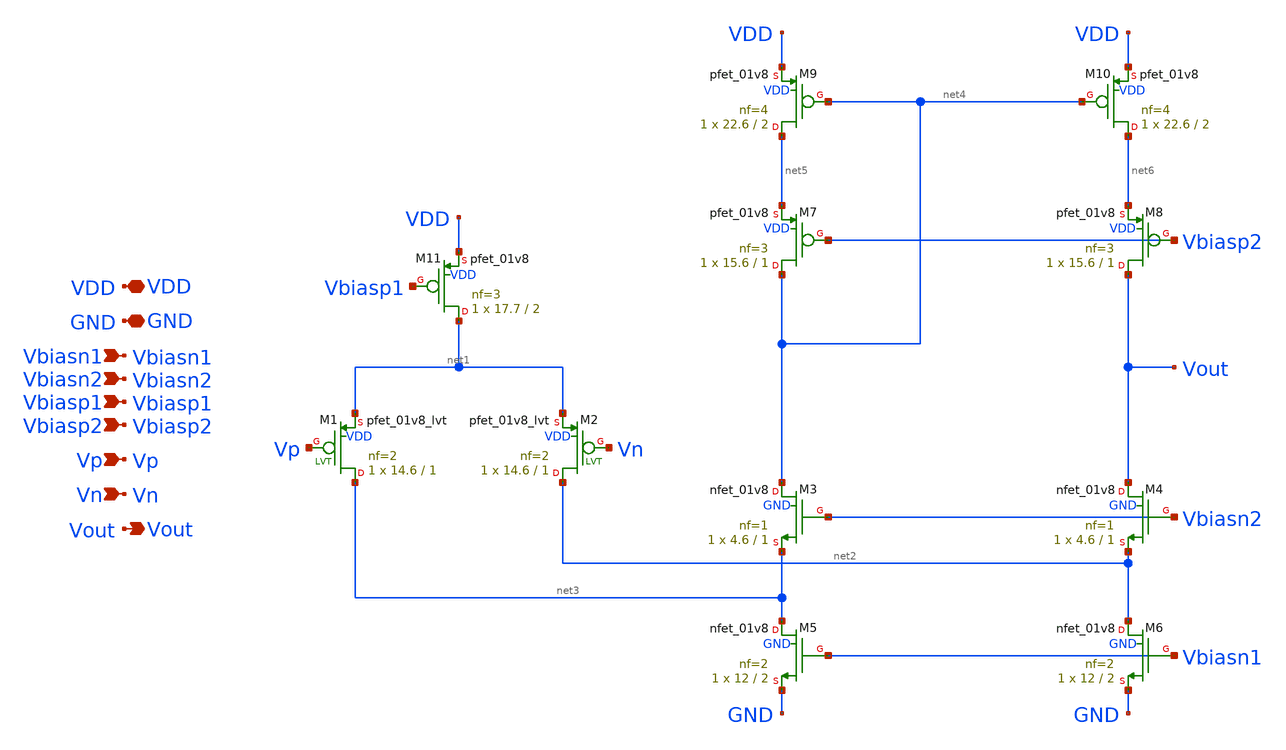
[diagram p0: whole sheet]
** sch_path: sch/vi_converter/ota_vi.sch
**.subckt ota_vi Vbiasn2 Vout VDD GND Vp Vn Vbiasp1 Vbiasp2 Vbiasn1
*.ipin Vbiasn2
*.opin Vout
*.iopin VDD
*.iopin GND
*.ipin Vp
*.ipin Vn
*.ipin Vbiasp1
*.ipin Vbiasp2
*.ipin Vbiasn1
XM3 net4 Vbiasn2 net3 GND sky130_fd_pr__nfet_01v8 L=1 W=4.6 nf=1 ad='int((1 + 1)/2) * 4.6 / 1 * 0.29'
+ as='int((1 + 2)/2) * 4.6 / 1 * 0.29' pd='2*int((1 + 1)/2) * (4.6 / 1 + 0.29)' ps='2*int((1 + 2)/2) * (4.6 / 1 + 0.29)'
+ nrd='0.29 / 4.6 ' nrs='0.29 / 4.6 ' sa=0 sb=0 sd=0 mult=1 m=1
XM4 Vout Vbiasn2 net2 GND sky130_fd_pr__nfet_01v8 L=1 W=4.6 nf=1 ad='int((1 + 1)/2) * 4.6 / 1 * 0.29'
+ as='int((1 + 2)/2) * 4.6 / 1 * 0.29' pd='2*int((1 + 1)/2) * (4.6 / 1 + 0.29)' ps='2*int((1 + 2)/2) * (4.6 / 1 + 0.29)'
+ nrd='0.29 / 4.6 ' nrs='0.29 / 4.6 ' sa=0 sb=0 sd=0 mult=1 m=1
XM5 net3 Vbiasn1 GND GND sky130_fd_pr__nfet_01v8 L=2 W=12 nf=2 ad='int((2 + 1)/2) * 12 / 2 * 0.29' as='int((2 + 2)/2) * 12 / 2 * 0.29'
+ pd='2*int((2 + 1)/2) * (12 / 2 + 0.29)' ps='2*int((2 + 2)/2) * (12 / 2 + 0.29)' nrd='0.29 / 12 ' nrs='0.29 / 12 '
+ sa=0 sb=0 sd=0 mult=1 m=1
XM6 net2 Vbiasn1 GND GND sky130_fd_pr__nfet_01v8 L=2 W=12 nf=2 ad='int((2 + 1)/2) * 12 / 2 * 0.29' as='int((2 + 2)/2) * 12 / 2 * 0.29'
+ pd='2*int((2 + 1)/2) * (12 / 2 + 0.29)' ps='2*int((2 + 2)/2) * (12 / 2 + 0.29)' nrd='0.29 / 12 ' nrs='0.29 / 12 '
+ sa=0 sb=0 sd=0 mult=1 m=1
XM7 net4 Vbiasp2 net5 VDD sky130_fd_pr__pfet_01v8 L=1 W=15.6 nf=3 ad='int((3 + 1)/2) * 15.6 / 3 * 0.29'
+ as='int((3 + 2)/2) * 15.6 / 3 * 0.29' pd='2*int((3 + 1)/2) * (15.6 / 3 + 0.29)' ps='2*int((3 + 2)/2) * (15.6 / 3 + 0.29)'
+ nrd='0.29 / 15.6 ' nrs='0.29 / 15.6 ' sa=0 sb=0 sd=0 mult=1 m=1
XM8 Vout Vbiasp2 net6 VDD sky130_fd_pr__pfet_01v8 L=1 W=15.6 nf=3 ad='int((3 + 1)/2) * 15.6 / 3 * 0.29'
+ as='int((3 + 2)/2) * 15.6 / 3 * 0.29' pd='2*int((3 + 1)/2) * (15.6 / 3 + 0.29)' ps='2*int((3 + 2)/2) * (15.6 / 3 + 0.29)'
+ nrd='0.29 / 15.6 ' nrs='0.29 / 15.6 ' sa=0 sb=0 sd=0 mult=1 m=1
XM9 net5 net4 VDD VDD sky130_fd_pr__pfet_01v8 L=2 W=22.6 nf=4 ad='int((4 + 1)/2) * 22.6 / 4 * 0.29' as='int((4 + 2)/2) * 22.6 / 4 * 0.29'
+ pd='2*int((4 + 1)/2) * (22.6 / 4 + 0.29)' ps='2*int((4 + 2)/2) * (22.6 / 4 + 0.29)' nrd='0.29 / 22.6 '
+ nrs='0.29 / 22.6 ' sa=0 sb=0 sd=0 mult=1 m=1
XM10 net6 net4 VDD VDD sky130_fd_pr__pfet_01v8 L=2 W=22.6 nf=4 ad='int((4 + 1)/2) * 22.6 / 4 * 0.29'
+ as='int((4 + 2)/2) * 22.6 / 4 * 0.29' pd='2*int((4 + 1)/2) * (22.6 / 4 + 0.29)' ps='2*int((4 + 2)/2) * (22.6 / 4 + 0.29)'
+ nrd='0.29 / 22.6 ' nrs='0.29 / 22.6 ' sa=0 sb=0 sd=0 mult=1 m=1
XM11 net1 Vbiasp1 VDD VDD sky130_fd_pr__pfet_01v8 L=2 W=17.7 nf=3 ad='int((3 + 1)/2) * 17.7 / 3 * 0.29'
+ as='int((3 + 2)/2) * 17.7 / 3 * 0.29' pd='2*int((3 + 1)/2) * (17.7 / 3 + 0.29)' ps='2*int((3 + 2)/2) * (17.7 / 3 + 0.29)'
+ nrd='0.29 / 17.7 ' nrs='0.29 / 17.7 ' sa=0 sb=0 sd=0 mult=1 m=1
XM1 net3 Vp net1 VDD sky130_fd_pr__pfet_01v8_lvt L=1 W=14.6 nf=2 ad='int((2 + 1)/2) * 14.6 / 2 * 0.29'
+ as='int((2 + 2)/2) * 14.6 / 2 * 0.29' pd='2*int((2 + 1)/2) * (14.6 / 2 + 0.29)' ps='2*int((2 + 2)/2) * (14.6 / 2 + 0.29)'
+ nrd='0.29 / 14.6 ' nrs='0.29 / 14.6 ' sa=0 sb=0 sd=0 mult=1 m=1
XM2 net2 Vn net1 VDD sky130_fd_pr__pfet_01v8_lvt L=1 W=14.6 nf=2 ad='int((2 + 1)/2) * 14.6 / 2 * 0.29'
+ as='int((2 + 2)/2) * 14.6 / 2 * 0.29' pd='2*int((2 + 1)/2) * (14.6 / 2 + 0.29)' ps='2*int((2 + 2)/2) * (14.6 / 2 + 0.29)'
+ nrd='0.29 / 14.6 ' nrs='0.29 / 14.6 ' sa=0 sb=0 sd=0 mult=1 m=1
**.ends
.end
